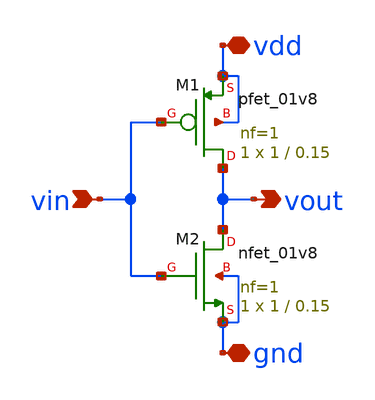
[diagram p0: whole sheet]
** sch_path: hopfield/inverter.sch
**.subckt inverter vin vdd vout gnd
*.ipin vin
*.iopin vdd
*.opin vout
*.iopin gnd
XM1 vout vin vdd vdd sky130_fd_pr__pfet_01v8 L=0.15 W=1 nf=1 ad='int((nf+1)/2) * W/nf * 0.29' as='int((nf+2)/2) * W/nf * 0.29'
+ pd='2*int((nf+1)/2) * (W/nf + 0.29)' ps='2*int((nf+2)/2) * (W/nf + 0.29)' nrd='0.29 / W' nrs='0.29 / W'
+ sa=0 sb=0 sd=0 mult=1 m=1
XM2 vout vin gnd gnd sky130_fd_pr__nfet_01v8 L=0.15 W=1 nf=1 ad='int((nf+1)/2) * W/nf * 0.29' as='int((nf+2)/2) * W/nf * 0.29'
+ pd='2*int((nf+1)/2) * (W/nf + 0.29)' ps='2*int((nf+2)/2) * (W/nf + 0.29)' nrd='0.29 / W' nrs='0.29 / W'
+ sa=0 sb=0 sd=0 mult=1 m=1
**.ends
.end
